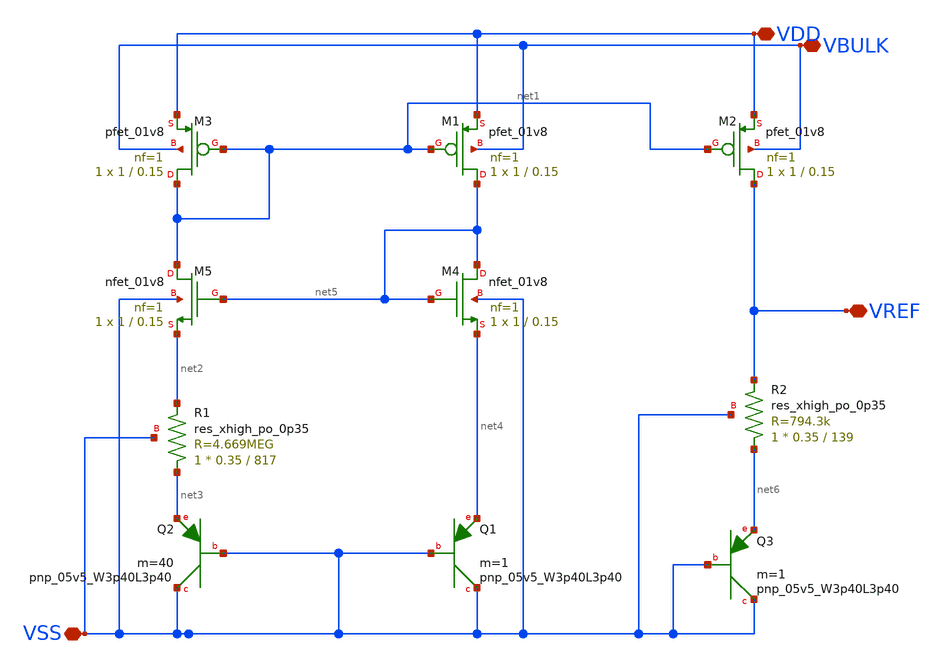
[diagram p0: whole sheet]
** sch_path: xschem/bandgap_1.sch
**.subckt bandgap_1 VDD VBULK VSS VREF
*.iopin VDD
*.iopin VBULK
*.iopin VSS
*.iopin VREF
XM1 net5 net1 VDD VBULK sky130_fd_pr__pfet_01v8 L=0.15 W=1 nf=1 ad='int((nf+1)/2) * W/nf * 0.29' as='int((nf+2)/2) * W/nf * 0.29'
+ pd='2*int((nf+1)/2) * (W/nf + 0.29)' ps='2*int((nf+2)/2) * (W/nf + 0.29)' nrd='0.29 / W' nrs='0.29 / W'
+ sa=0 sb=0 sd=0 mult=1 m=1
XM2 VREF net1 VDD VBULK sky130_fd_pr__pfet_01v8 L=0.15 W=1 nf=1 ad='int((nf+1)/2) * W/nf * 0.29' as='int((nf+2)/2) * W/nf * 0.29'
+ pd='2*int((nf+1)/2) * (W/nf + 0.29)' ps='2*int((nf+2)/2) * (W/nf + 0.29)' nrd='0.29 / W' nrs='0.29 / W'
+ sa=0 sb=0 sd=0 mult=1 m=1
XM3 net1 net1 VDD VBULK sky130_fd_pr__pfet_01v8 L=0.15 W=1 nf=1 ad='int((nf+1)/2) * W/nf * 0.29' as='int((nf+2)/2) * W/nf * 0.29'
+ pd='2*int((nf+1)/2) * (W/nf + 0.29)' ps='2*int((nf+2)/2) * (W/nf + 0.29)' nrd='0.29 / W' nrs='0.29 / W'
+ sa=0 sb=0 sd=0 mult=1 m=1
XM4 net5 net5 net4 VSS sky130_fd_pr__nfet_01v8 L=0.15 W=1 nf=1 ad='int((nf+1)/2) * W/nf * 0.29' as='int((nf+2)/2) * W/nf * 0.29'
+ pd='2*int((nf+1)/2) * (W/nf + 0.29)' ps='2*int((nf+2)/2) * (W/nf + 0.29)' nrd='0.29 / W' nrs='0.29 / W'
+ sa=0 sb=0 sd=0 mult=1 m=1
XM5 net1 net5 net2 VSS sky130_fd_pr__nfet_01v8 L=0.15 W=1 nf=1 ad='int((nf+1)/2) * W/nf * 0.29' as='int((nf+2)/2) * W/nf * 0.29'
+ pd='2*int((nf+1)/2) * (W/nf + 0.29)' ps='2*int((nf+2)/2) * (W/nf + 0.29)' nrd='0.29 / W' nrs='0.29 / W'
+ sa=0 sb=0 sd=0 mult=1 m=1
XQ1 VSS VSS net4 sky130_fd_pr__pnp_05v5_W3p40L3p40 m=1
XQ2 VSS VSS net3 sky130_fd_pr__pnp_05v5_W3p40L3p40 m=40
XR1 net3 net2 VSS sky130_fd_pr__res_xhigh_po_0p35 L=817 mult=1 m=1
XR2 net6 VREF VSS sky130_fd_pr__res_xhigh_po_0p35 L=139 mult=1 m=1
XQ3 VSS VSS net6 sky130_fd_pr__pnp_05v5_W3p40L3p40 m=1
**.ends
.end
